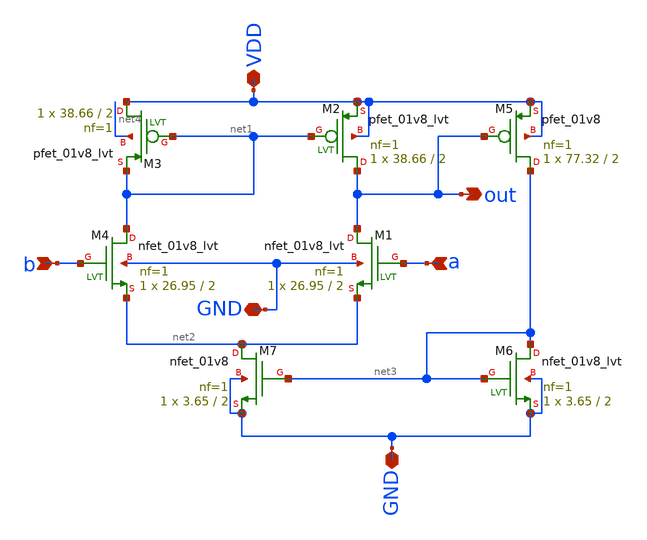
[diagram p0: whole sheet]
** sch_path: schematic/amplifier_self_bias.sch
**.subckt amplifier_self_bias b GND GND a VDD out
*.ipin b
*.iopin GND
*.iopin GND
*.ipin a
*.iopin VDD
*.opin out
XM1 out a net2 GND sky130_fd_pr__nfet_01v8_lvt L=2 W=26.95 nf=1 ad='int((nf+1)/2) * W/nf * 0.29' as='int((nf+2)/2) * W/nf * 0.29'
+ pd='2*int((nf+1)/2) * (W/nf + 0.29)' ps='2*int((nf+2)/2) * (W/nf + 0.29)' nrd='0.29 / W' nrs='0.29 / W'
+ sa=0 sb=0 sd=0 mult=1 m=1
XM2 out net1 VDD VDD sky130_fd_pr__pfet_01v8_lvt L=2 W=38.66 nf=1 ad='int((nf+1)/2) * W/nf * 0.29' as='int((nf+2)/2) * W/nf * 0.29'
+ pd='2*int((nf+1)/2) * (W/nf + 0.29)' ps='2*int((nf+2)/2) * (W/nf + 0.29)' nrd='0.29 / W' nrs='0.29 / W'
+ sa=0 sb=0 sd=0 mult=1 m=1
XM3 VDD net1 net1 net4 sky130_fd_pr__pfet_01v8_lvt L=2 W=38.66 nf=1 ad='int((nf+1)/2) * W/nf * 0.29'
+ as='int((nf+2)/2) * W/nf * 0.29' pd='2*int((nf+1)/2) * (W/nf + 0.29)' ps='2*int((nf+2)/2) * (W/nf + 0.29)'
+ nrd='0.29 / W' nrs='0.29 / W' sa=0 sb=0 sd=0 mult=1 m=1
XM4 net1 b net2 GND sky130_fd_pr__nfet_01v8_lvt L=2 W=26.95 nf=1 ad='int((nf+1)/2) * W/nf * 0.29' as='int((nf+2)/2) * W/nf * 0.29'
+ pd='2*int((nf+1)/2) * (W/nf + 0.29)' ps='2*int((nf+2)/2) * (W/nf + 0.29)' nrd='0.29 / W' nrs='0.29 / W'
+ sa=0 sb=0 sd=0 mult=1 m=1
XM5 net3 out VDD VDD sky130_fd_pr__pfet_01v8 L=2 W=77.32 nf=1 ad='int((nf+1)/2) * W/nf * 0.29' as='int((nf+2)/2) * W/nf * 0.29'
+ pd='2*int((nf+1)/2) * (W/nf + 0.29)' ps='2*int((nf+2)/2) * (W/nf + 0.29)' nrd='0.29 / W' nrs='0.29 / W'
+ sa=0 sb=0 sd=0 mult=1 m=1
XM6 net3 net3 GND GND sky130_fd_pr__nfet_01v8_lvt L=2 W=3.65 nf=1 ad='int((nf+1)/2) * W/nf * 0.29' as='int((nf+2)/2) * W/nf * 0.29'
+ pd='2*int((nf+1)/2) * (W/nf + 0.29)' ps='2*int((nf+2)/2) * (W/nf + 0.29)' nrd='0.29 / W' nrs='0.29 / W'
+ sa=0 sb=0 sd=0 mult=1 m=1
XM7 net2 net3 GND GND sky130_fd_pr__nfet_01v8 L=2 W=3.65 nf=1 ad='int((nf+1)/2) * W/nf * 0.29' as='int((nf+2)/2) * W/nf * 0.29'
+ pd='2*int((nf+1)/2) * (W/nf + 0.29)' ps='2*int((nf+2)/2) * (W/nf + 0.29)' nrd='0.29 / W' nrs='0.29 / W'
+ sa=0 sb=0 sd=0 mult=1 m=1
**.ends
.end
